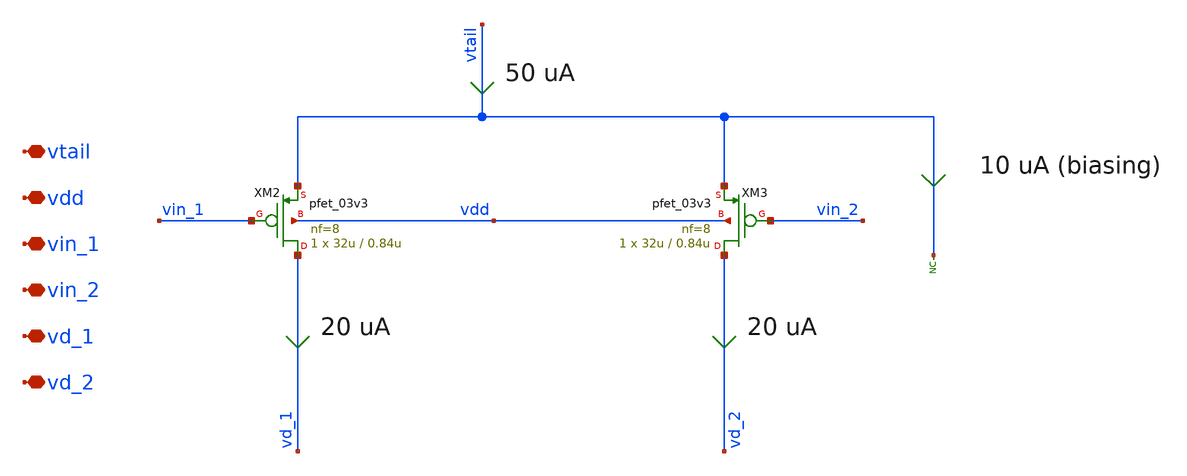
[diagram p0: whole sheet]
** sch_path: xschem/ccia_rrl_ota/b9_ccia_rrl_ota_input_pair.sch
**.subckt b9_ccia_rrl_ota_input_pair vtail vdd vin_1 vin_2 vd_1 vd_2
*.iopin vtail
*.iopin vdd
*.iopin vin_1
*.iopin vin_2
*.iopin vd_1
*.iopin vd_2
XM2 vd_1 vin_1 vtail vdd pfet_03v3 L=0.84u W=32u nf=8 ad='int((nf+1)/2) * W/nf * 0.18u' as='int((nf+2)/2) * W/nf * 0.18u'
+ pd='2*int((nf+1)/2) * (W/nf + 0.18u)' ps='2*int((nf+2)/2) * (W/nf + 0.18u)' nrd='0.18u / W' nrs='0.18u / W'
+ sa=0 sb=0 sd=0 m=1
XM3 vd_2 vin_2 vtail vdd pfet_03v3 L=0.84u W=32u nf=8 ad='int((nf+1)/2) * W/nf * 0.18u' as='int((nf+2)/2) * W/nf * 0.18u'
+ pd='2*int((nf+1)/2) * (W/nf + 0.18u)' ps='2*int((nf+2)/2) * (W/nf + 0.18u)' nrd='0.18u / W' nrs='0.18u / W'
+ sa=0 sb=0 sd=0 m=1
* noconn vtail
**.ends
.end
